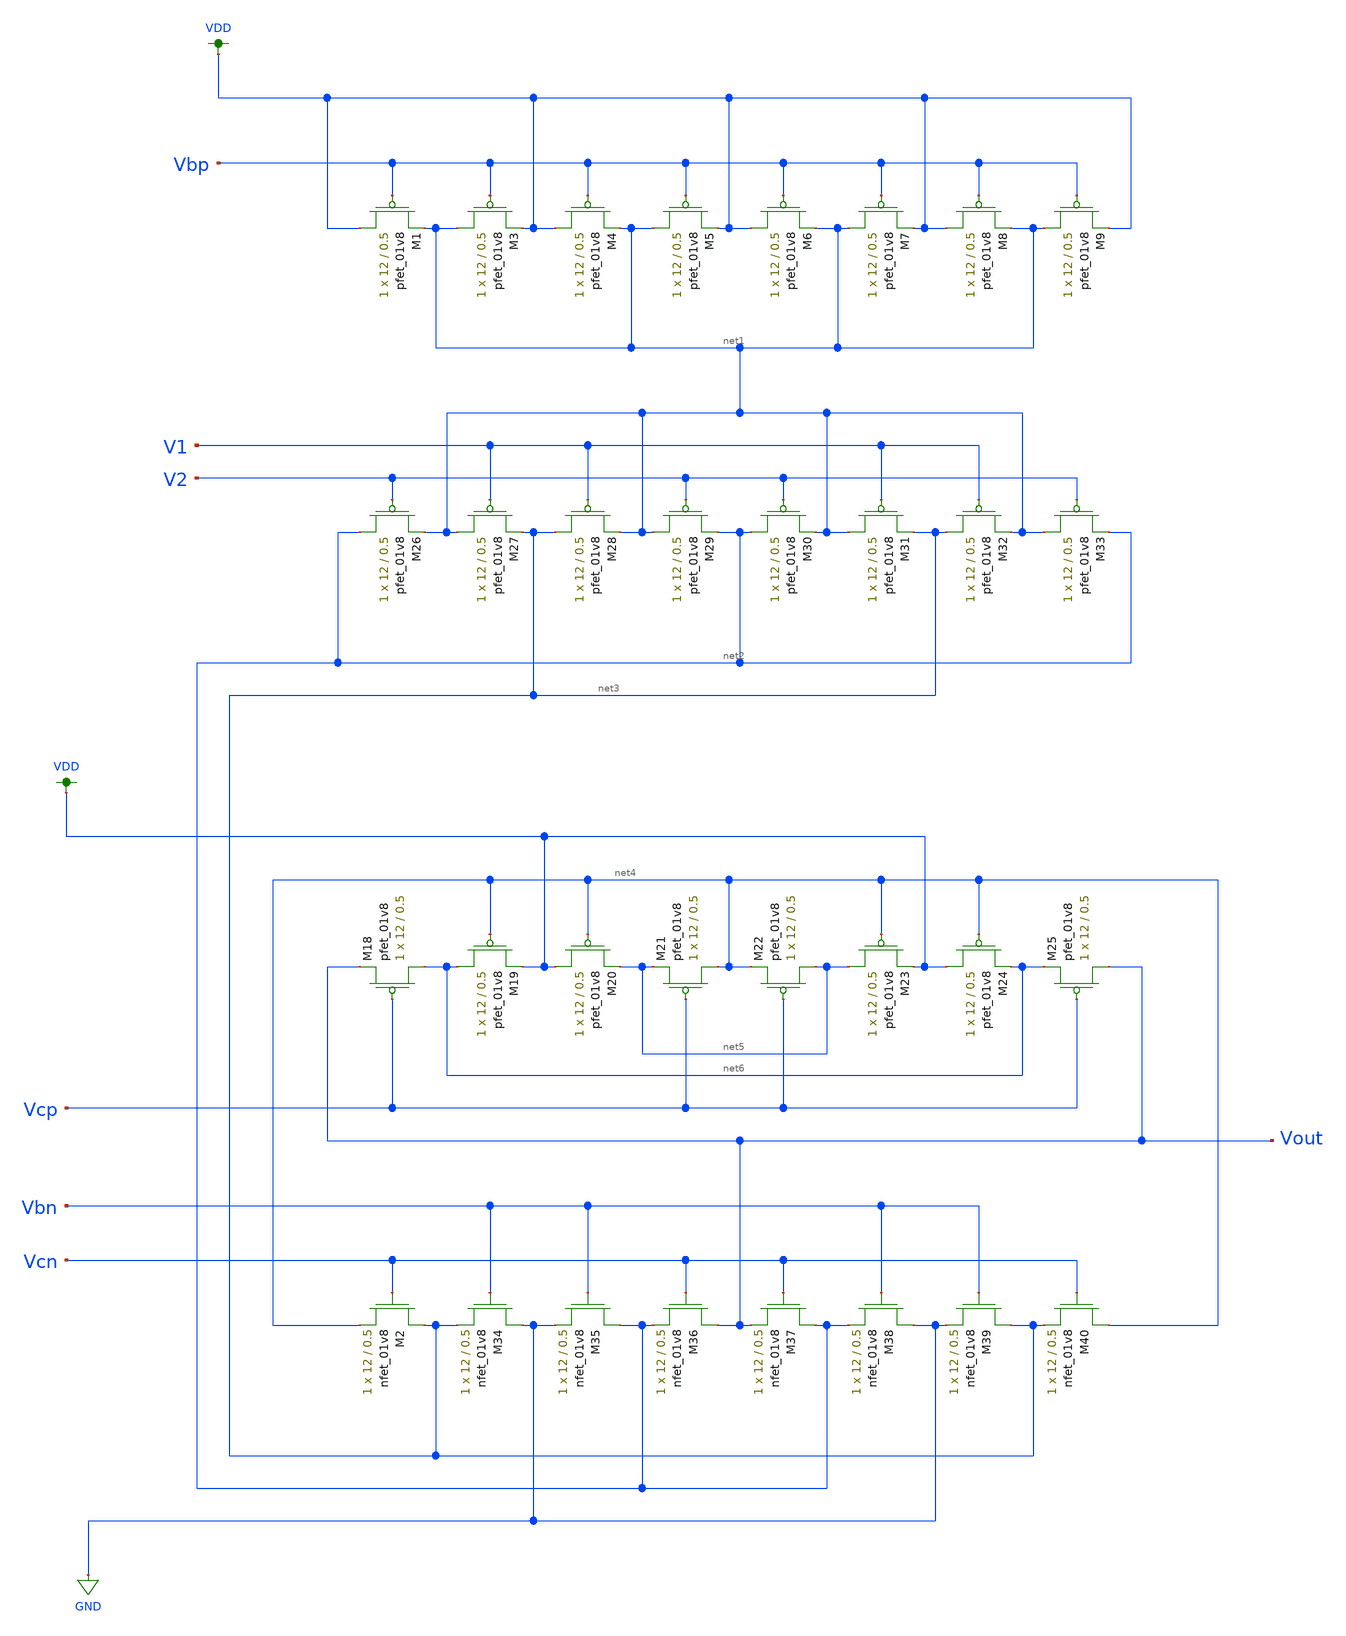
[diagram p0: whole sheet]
** sch_path: MP3/cascode-lds.sch
**.subckt cascode-lds
XM1 VDD Vbp net1 VDD sky130_fd_pr__pfet_01v8 L=0.5 W=12 nf=1 ad='int((nf+1)/2) * W/nf * 0.29' as='int((nf+2)/2) * W/nf * 0.29'
+ pd='2*int((nf+1)/2) * (W/nf + 0.29)' ps='2*int((nf+2)/2) * (W/nf + 0.29)' nrd='0.29 / W' nrs='0.29 / W'
+ sa=0 sb=0 sd=0 mult=1 m=1
XM2 net3 Vcn net4 GND sky130_fd_pr__nfet_01v8 L=0.5 W=12 nf=1 ad='int((nf+1)/2) * W/nf * 0.29' as='int((nf+2)/2) * W/nf * 0.29'
+ pd='2*int((nf+1)/2) * (W/nf + 0.29)' ps='2*int((nf+2)/2) * (W/nf + 0.29)' nrd='0.29 / W' nrs='0.29 / W'
+ sa=0 sb=0 sd=0 mult=1 m=1
XM3 net1 Vbp VDD VDD sky130_fd_pr__pfet_01v8 L=0.5 W=12 nf=1 ad='int((nf+1)/2) * W/nf * 0.29' as='int((nf+2)/2) * W/nf * 0.29'
+ pd='2*int((nf+1)/2) * (W/nf + 0.29)' ps='2*int((nf+2)/2) * (W/nf + 0.29)' nrd='0.29 / W' nrs='0.29 / W'
+ sa=0 sb=0 sd=0 mult=1 m=1
XM4 VDD Vbp net1 VDD sky130_fd_pr__pfet_01v8 L=0.5 W=12 nf=1 ad='int((nf+1)/2) * W/nf * 0.29' as='int((nf+2)/2) * W/nf * 0.29'
+ pd='2*int((nf+1)/2) * (W/nf + 0.29)' ps='2*int((nf+2)/2) * (W/nf + 0.29)' nrd='0.29 / W' nrs='0.29 / W'
+ sa=0 sb=0 sd=0 mult=1 m=1
XM5 net1 Vbp VDD VDD sky130_fd_pr__pfet_01v8 L=0.5 W=12 nf=1 ad='int((nf+1)/2) * W/nf * 0.29' as='int((nf+2)/2) * W/nf * 0.29'
+ pd='2*int((nf+1)/2) * (W/nf + 0.29)' ps='2*int((nf+2)/2) * (W/nf + 0.29)' nrd='0.29 / W' nrs='0.29 / W'
+ sa=0 sb=0 sd=0 mult=1 m=1
XM6 VDD Vbp net1 VDD sky130_fd_pr__pfet_01v8 L=0.5 W=12 nf=1 ad='int((nf+1)/2) * W/nf * 0.29' as='int((nf+2)/2) * W/nf * 0.29'
+ pd='2*int((nf+1)/2) * (W/nf + 0.29)' ps='2*int((nf+2)/2) * (W/nf + 0.29)' nrd='0.29 / W' nrs='0.29 / W'
+ sa=0 sb=0 sd=0 mult=1 m=1
XM7 net1 Vbp VDD VDD sky130_fd_pr__pfet_01v8 L=0.5 W=12 nf=1 ad='int((nf+1)/2) * W/nf * 0.29' as='int((nf+2)/2) * W/nf * 0.29'
+ pd='2*int((nf+1)/2) * (W/nf + 0.29)' ps='2*int((nf+2)/2) * (W/nf + 0.29)' nrd='0.29 / W' nrs='0.29 / W'
+ sa=0 sb=0 sd=0 mult=1 m=1
XM8 VDD Vbp net1 VDD sky130_fd_pr__pfet_01v8 L=0.5 W=12 nf=1 ad='int((nf+1)/2) * W/nf * 0.29' as='int((nf+2)/2) * W/nf * 0.29'
+ pd='2*int((nf+1)/2) * (W/nf + 0.29)' ps='2*int((nf+2)/2) * (W/nf + 0.29)' nrd='0.29 / W' nrs='0.29 / W'
+ sa=0 sb=0 sd=0 mult=1 m=1
XM9 net1 Vbp VDD VDD sky130_fd_pr__pfet_01v8 L=0.5 W=12 nf=1 ad='int((nf+1)/2) * W/nf * 0.29' as='int((nf+2)/2) * W/nf * 0.29'
+ pd='2*int((nf+1)/2) * (W/nf + 0.29)' ps='2*int((nf+2)/2) * (W/nf + 0.29)' nrd='0.29 / W' nrs='0.29 / W'
+ sa=0 sb=0 sd=0 mult=1 m=1
XM18 net6 Vcp Vout VDD sky130_fd_pr__pfet_01v8 L=0.5 W=12 nf=1 ad='int((nf+1)/2) * W/nf * 0.29' as='int((nf+2)/2) * W/nf * 0.29'
+ pd='2*int((nf+1)/2) * (W/nf + 0.29)' ps='2*int((nf+2)/2) * (W/nf + 0.29)' nrd='0.29 / W' nrs='0.29 / W'
+ sa=0 sb=0 sd=0 mult=1 m=1
XM19 net6 net4 VDD VDD sky130_fd_pr__pfet_01v8 L=0.5 W=12 nf=1 ad='int((nf+1)/2) * W/nf * 0.29' as='int((nf+2)/2) * W/nf * 0.29'
+ pd='2*int((nf+1)/2) * (W/nf + 0.29)' ps='2*int((nf+2)/2) * (W/nf + 0.29)' nrd='0.29 / W' nrs='0.29 / W'
+ sa=0 sb=0 sd=0 mult=1 m=1
XM20 VDD net4 net5 VDD sky130_fd_pr__pfet_01v8 L=0.5 W=12 nf=1 ad='int((nf+1)/2) * W/nf * 0.29' as='int((nf+2)/2) * W/nf * 0.29'
+ pd='2*int((nf+1)/2) * (W/nf + 0.29)' ps='2*int((nf+2)/2) * (W/nf + 0.29)' nrd='0.29 / W' nrs='0.29 / W'
+ sa=0 sb=0 sd=0 mult=1 m=1
XM21 net4 Vcp net5 VDD sky130_fd_pr__pfet_01v8 L=0.5 W=12 nf=1 ad='int((nf+1)/2) * W/nf * 0.29' as='int((nf+2)/2) * W/nf * 0.29'
+ pd='2*int((nf+1)/2) * (W/nf + 0.29)' ps='2*int((nf+2)/2) * (W/nf + 0.29)' nrd='0.29 / W' nrs='0.29 / W'
+ sa=0 sb=0 sd=0 mult=1 m=1
XM22 net5 Vcp net4 VDD sky130_fd_pr__pfet_01v8 L=0.5 W=12 nf=1 ad='int((nf+1)/2) * W/nf * 0.29' as='int((nf+2)/2) * W/nf * 0.29'
+ pd='2*int((nf+1)/2) * (W/nf + 0.29)' ps='2*int((nf+2)/2) * (W/nf + 0.29)' nrd='0.29 / W' nrs='0.29 / W'
+ sa=0 sb=0 sd=0 mult=1 m=1
XM23 net5 net4 VDD VDD sky130_fd_pr__pfet_01v8 L=0.5 W=12 nf=1 ad='int((nf+1)/2) * W/nf * 0.29' as='int((nf+2)/2) * W/nf * 0.29'
+ pd='2*int((nf+1)/2) * (W/nf + 0.29)' ps='2*int((nf+2)/2) * (W/nf + 0.29)' nrd='0.29 / W' nrs='0.29 / W'
+ sa=0 sb=0 sd=0 mult=1 m=1
XM24 VDD net4 net6 VDD sky130_fd_pr__pfet_01v8 L=0.5 W=12 nf=1 ad='int((nf+1)/2) * W/nf * 0.29' as='int((nf+2)/2) * W/nf * 0.29'
+ pd='2*int((nf+1)/2) * (W/nf + 0.29)' ps='2*int((nf+2)/2) * (W/nf + 0.29)' nrd='0.29 / W' nrs='0.29 / W'
+ sa=0 sb=0 sd=0 mult=1 m=1
XM25 Vout Vcp net6 VDD sky130_fd_pr__pfet_01v8 L=0.5 W=12 nf=1 ad='int((nf+1)/2) * W/nf * 0.29' as='int((nf+2)/2) * W/nf * 0.29'
+ pd='2*int((nf+1)/2) * (W/nf + 0.29)' ps='2*int((nf+2)/2) * (W/nf + 0.29)' nrd='0.29 / W' nrs='0.29 / W'
+ sa=0 sb=0 sd=0 mult=1 m=1
XM26 net2 V2 net1 VDD sky130_fd_pr__pfet_01v8 L=0.5 W=12 nf=1 ad='int((nf+1)/2) * W/nf * 0.29' as='int((nf+2)/2) * W/nf * 0.29'
+ pd='2*int((nf+1)/2) * (W/nf + 0.29)' ps='2*int((nf+2)/2) * (W/nf + 0.29)' nrd='0.29 / W' nrs='0.29 / W'
+ sa=0 sb=0 sd=0 mult=1 m=1
XM27 net1 V1 net3 VDD sky130_fd_pr__pfet_01v8 L=0.5 W=12 nf=1 ad='int((nf+1)/2) * W/nf * 0.29' as='int((nf+2)/2) * W/nf * 0.29'
+ pd='2*int((nf+1)/2) * (W/nf + 0.29)' ps='2*int((nf+2)/2) * (W/nf + 0.29)' nrd='0.29 / W' nrs='0.29 / W'
+ sa=0 sb=0 sd=0 mult=1 m=1
XM28 net3 V1 net1 VDD sky130_fd_pr__pfet_01v8 L=0.5 W=12 nf=1 ad='int((nf+1)/2) * W/nf * 0.29' as='int((nf+2)/2) * W/nf * 0.29'
+ pd='2*int((nf+1)/2) * (W/nf + 0.29)' ps='2*int((nf+2)/2) * (W/nf + 0.29)' nrd='0.29 / W' nrs='0.29 / W'
+ sa=0 sb=0 sd=0 mult=1 m=1
XM29 net1 V2 net2 VDD sky130_fd_pr__pfet_01v8 L=0.5 W=12 nf=1 ad='int((nf+1)/2) * W/nf * 0.29' as='int((nf+2)/2) * W/nf * 0.29'
+ pd='2*int((nf+1)/2) * (W/nf + 0.29)' ps='2*int((nf+2)/2) * (W/nf + 0.29)' nrd='0.29 / W' nrs='0.29 / W'
+ sa=0 sb=0 sd=0 mult=1 m=1
XM30 net2 V2 net1 VDD sky130_fd_pr__pfet_01v8 L=0.5 W=12 nf=1 ad='int((nf+1)/2) * W/nf * 0.29' as='int((nf+2)/2) * W/nf * 0.29'
+ pd='2*int((nf+1)/2) * (W/nf + 0.29)' ps='2*int((nf+2)/2) * (W/nf + 0.29)' nrd='0.29 / W' nrs='0.29 / W'
+ sa=0 sb=0 sd=0 mult=1 m=1
XM31 net1 V1 net3 VDD sky130_fd_pr__pfet_01v8 L=0.5 W=12 nf=1 ad='int((nf+1)/2) * W/nf * 0.29' as='int((nf+2)/2) * W/nf * 0.29'
+ pd='2*int((nf+1)/2) * (W/nf + 0.29)' ps='2*int((nf+2)/2) * (W/nf + 0.29)' nrd='0.29 / W' nrs='0.29 / W'
+ sa=0 sb=0 sd=0 mult=1 m=1
XM32 net3 V1 net1 VDD sky130_fd_pr__pfet_01v8 L=0.5 W=12 nf=1 ad='int((nf+1)/2) * W/nf * 0.29' as='int((nf+2)/2) * W/nf * 0.29'
+ pd='2*int((nf+1)/2) * (W/nf + 0.29)' ps='2*int((nf+2)/2) * (W/nf + 0.29)' nrd='0.29 / W' nrs='0.29 / W'
+ sa=0 sb=0 sd=0 mult=1 m=1
XM33 net1 V2 net2 VDD sky130_fd_pr__pfet_01v8 L=0.5 W=12 nf=1 ad='int((nf+1)/2) * W/nf * 0.29' as='int((nf+2)/2) * W/nf * 0.29'
+ pd='2*int((nf+1)/2) * (W/nf + 0.29)' ps='2*int((nf+2)/2) * (W/nf + 0.29)' nrd='0.29 / W' nrs='0.29 / W'
+ sa=0 sb=0 sd=0 mult=1 m=1
XM34 GND Vbn net3 GND sky130_fd_pr__nfet_01v8 L=0.5 W=12 nf=1 ad='int((nf+1)/2) * W/nf * 0.29' as='int((nf+2)/2) * W/nf * 0.29'
+ pd='2*int((nf+1)/2) * (W/nf + 0.29)' ps='2*int((nf+2)/2) * (W/nf + 0.29)' nrd='0.29 / W' nrs='0.29 / W'
+ sa=0 sb=0 sd=0 mult=1 m=1
XM35 net2 Vbn GND GND sky130_fd_pr__nfet_01v8 L=0.5 W=12 nf=1 ad='int((nf+1)/2) * W/nf * 0.29' as='int((nf+2)/2) * W/nf * 0.29'
+ pd='2*int((nf+1)/2) * (W/nf + 0.29)' ps='2*int((nf+2)/2) * (W/nf + 0.29)' nrd='0.29 / W' nrs='0.29 / W'
+ sa=0 sb=0 sd=0 mult=1 m=1
XM36 Vout Vcn net2 GND sky130_fd_pr__nfet_01v8 L=0.5 W=12 nf=1 ad='int((nf+1)/2) * W/nf * 0.29' as='int((nf+2)/2) * W/nf * 0.29'
+ pd='2*int((nf+1)/2) * (W/nf + 0.29)' ps='2*int((nf+2)/2) * (W/nf + 0.29)' nrd='0.29 / W' nrs='0.29 / W'
+ sa=0 sb=0 sd=0 mult=1 m=1
XM37 net2 Vcn Vout GND sky130_fd_pr__nfet_01v8 L=0.5 W=12 nf=1 ad='int((nf+1)/2) * W/nf * 0.29' as='int((nf+2)/2) * W/nf * 0.29'
+ pd='2*int((nf+1)/2) * (W/nf + 0.29)' ps='2*int((nf+2)/2) * (W/nf + 0.29)' nrd='0.29 / W' nrs='0.29 / W'
+ sa=0 sb=0 sd=0 mult=1 m=1
XM38 GND Vbn net2 GND sky130_fd_pr__nfet_01v8 L=0.5 W=12 nf=1 ad='int((nf+1)/2) * W/nf * 0.29' as='int((nf+2)/2) * W/nf * 0.29'
+ pd='2*int((nf+1)/2) * (W/nf + 0.29)' ps='2*int((nf+2)/2) * (W/nf + 0.29)' nrd='0.29 / W' nrs='0.29 / W'
+ sa=0 sb=0 sd=0 mult=1 m=1
XM39 net3 Vbn GND GND sky130_fd_pr__nfet_01v8 L=0.5 W=12 nf=1 ad='int((nf+1)/2) * W/nf * 0.29' as='int((nf+2)/2) * W/nf * 0.29'
+ pd='2*int((nf+1)/2) * (W/nf + 0.29)' ps='2*int((nf+2)/2) * (W/nf + 0.29)' nrd='0.29 / W' nrs='0.29 / W'
+ sa=0 sb=0 sd=0 mult=1 m=1
XM40 net4 Vcn net3 GND sky130_fd_pr__nfet_01v8 L=0.5 W=12 nf=1 ad='int((nf+1)/2) * W/nf * 0.29' as='int((nf+2)/2) * W/nf * 0.29'
+ pd='2*int((nf+1)/2) * (W/nf + 0.29)' ps='2*int((nf+2)/2) * (W/nf + 0.29)' nrd='0.29 / W' nrs='0.29 / W'
+ sa=0 sb=0 sd=0 mult=1 m=1
**.ends
.GLOBAL VDD
.GLOBAL GND
.end
